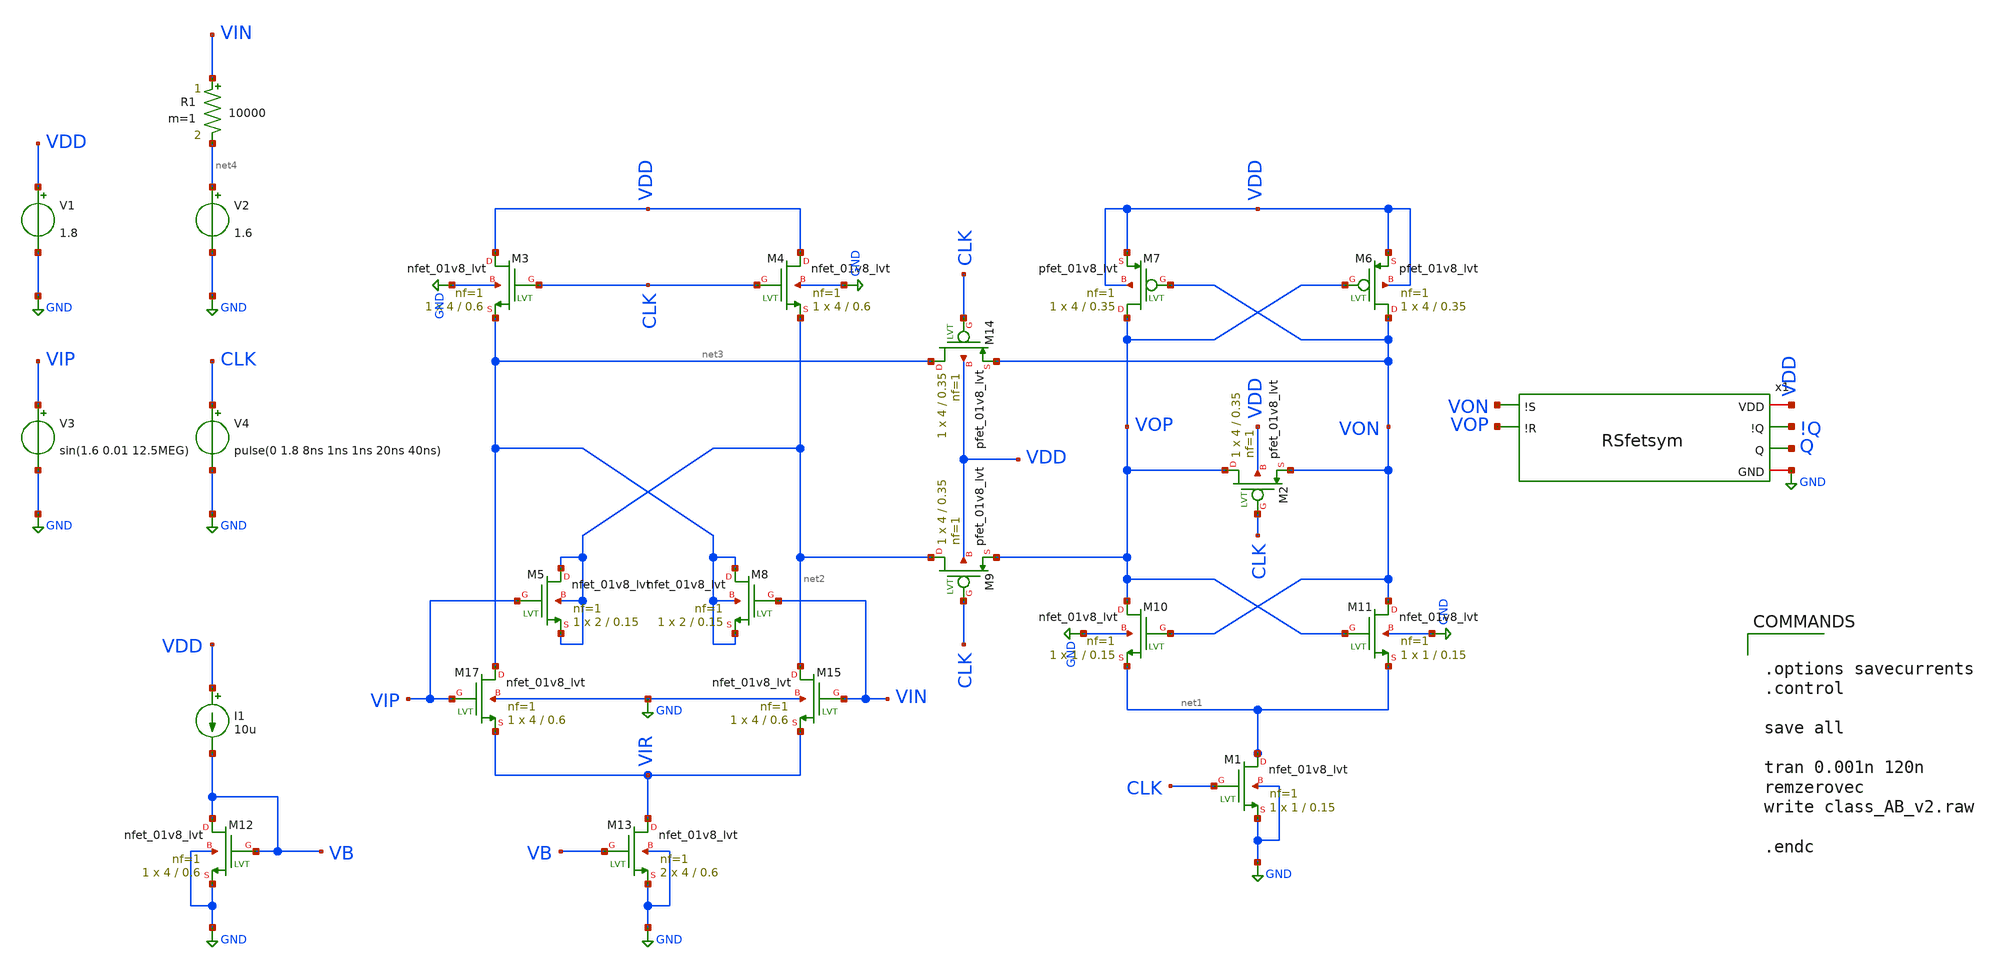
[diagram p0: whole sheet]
** sch_path: testbench/class_AB_v2.sch
.lib $::SKYWATER_MODELS/sky130.lib.spice tt
.include $::SKYWATER_STDCELLS/sky130_fd_sc_hd.spice

**.subckt class_AB_v2
XM17 net3 VIP VIR GND sky130_fd_pr__nfet_01v8_lvt L=0.6 W=4 nf=1 ad='int((nf+1)/2) * W/nf * 0.29' as='int((nf+2)/2) * W/nf * 0.29'
+ pd='2*int((nf+1)/2) * (W/nf + 0.29)' ps='2*int((nf+2)/2) * (W/nf + 0.29)' nrd='0.29 / W' nrs='0.29 / W'
+ sa=0 sb=0 sd=0 mult=1 m=1
XM12 VB VB GND GND sky130_fd_pr__nfet_01v8_lvt L=0.6 W=4 nf=1 ad='int((nf+1)/2) * W/nf * 0.29' as='int((nf+2)/2) * W/nf * 0.29'
+ pd='2*int((nf+1)/2) * (W/nf + 0.29)' ps='2*int((nf+2)/2) * (W/nf + 0.29)' nrd='0.29 / W' nrs='0.29 / W'
+ sa=0 sb=0 sd=0 mult=1 m=1
I1 VDD VB 10u
XM15 net2 VIN VIR GND sky130_fd_pr__nfet_01v8_lvt L=0.6 W=4 nf=1 ad='int((nf+1)/2) * W/nf * 0.29' as='int((nf+2)/2) * W/nf * 0.29'
+ pd='2*int((nf+1)/2) * (W/nf + 0.29)' ps='2*int((nf+2)/2) * (W/nf + 0.29)' nrd='0.29 / W' nrs='0.29 / W'
+ sa=0 sb=0 sd=0 mult=1 m=1
XM13 VIR VB GND GND sky130_fd_pr__nfet_01v8_lvt L=0.6 W=4 nf=1 ad='int((nf+1)/2) * W/nf * 0.29' as='int((nf+2)/2) * W/nf * 0.29'
+ pd='2*int((nf+1)/2) * (W/nf + 0.29)' ps='2*int((nf+2)/2) * (W/nf + 0.29)' nrd='0.29 / W' nrs='0.29 / W'
+ sa=0 sb=0 sd=0 mult=2 m=2
XM6 VON VOP VDD VDD sky130_fd_pr__pfet_01v8_lvt L=0.35 W=4 nf=1 ad='int((nf+1)/2) * W/nf * 0.29' as='int((nf+2)/2) * W/nf * 0.29'
+ pd='2*int((nf+1)/2) * (W/nf + 0.29)' ps='2*int((nf+2)/2) * (W/nf + 0.29)' nrd='0.29 / W' nrs='0.29 / W'
+ sa=0 sb=0 sd=0 mult=1 m=1
XM7 VOP VON VDD VDD sky130_fd_pr__pfet_01v8_lvt L=0.35 W=4 nf=1 ad='int((nf+1)/2) * W/nf * 0.29' as='int((nf+2)/2) * W/nf * 0.29'
+ pd='2*int((nf+1)/2) * (W/nf + 0.29)' ps='2*int((nf+2)/2) * (W/nf + 0.29)' nrd='0.29 / W' nrs='0.29 / W'
+ sa=0 sb=0 sd=0 mult=1 m=1
XM10 VOP VON net1 GND sky130_fd_pr__nfet_01v8_lvt L=0.15 W=1 nf=1 ad='int((nf+1)/2) * W/nf * 0.29' as='int((nf+2)/2) * W/nf * 0.29'
+ pd='2*int((nf+1)/2) * (W/nf + 0.29)' ps='2*int((nf+2)/2) * (W/nf + 0.29)' nrd='0.29 / W' nrs='0.29 / W'
+ sa=0 sb=0 sd=0 mult=1 m=1
XM11 VON VOP net1 GND sky130_fd_pr__nfet_01v8_lvt L=0.15 W=1 nf=1 ad='int((nf+1)/2) * W/nf * 0.29' as='int((nf+2)/2) * W/nf * 0.29'
+ pd='2*int((nf+1)/2) * (W/nf + 0.29)' ps='2*int((nf+2)/2) * (W/nf + 0.29)' nrd='0.29 / W' nrs='0.29 / W'
+ sa=0 sb=0 sd=0 mult=1 m=1
XM1 net1 CLK GND GND sky130_fd_pr__nfet_01v8_lvt L=0.15 W=1 nf=1 ad='int((nf+1)/2) * W/nf * 0.29' as='int((nf+2)/2) * W/nf * 0.29'
+ pd='2*int((nf+1)/2) * (W/nf + 0.29)' ps='2*int((nf+2)/2) * (W/nf + 0.29)' nrd='0.29 / W' nrs='0.29 / W'
+ sa=0 sb=0 sd=0 mult=1 m=1
XM2 VOP CLK VON VDD sky130_fd_pr__pfet_01v8_lvt L=0.35 W=4 nf=1 ad='int((nf+1)/2) * W/nf * 0.29' as='int((nf+2)/2) * W/nf * 0.29'
+ pd='2*int((nf+1)/2) * (W/nf + 0.29)' ps='2*int((nf+2)/2) * (W/nf + 0.29)' nrd='0.29 / W' nrs='0.29 / W'
+ sa=0 sb=0 sd=0 mult=1 m=1
V1 VDD GND 1.8
V3 VIP GND sin(1.6 0.01 12.5MEG)
V2 net4 GND 1.6
V4 CLK GND pulse(0 1.8 8ns 1ns 1ns 20ns 40ns)
R1 VIN net4 10000 m=1
XM5 net2 VIP net2 net2 sky130_fd_pr__nfet_01v8_lvt L=0.15 W=2 nf=1 ad='int((nf+1)/2) * W/nf * 0.29' as='int((nf+2)/2) * W/nf * 0.29'
+ pd='2*int((nf+1)/2) * (W/nf + 0.29)' ps='2*int((nf+2)/2) * (W/nf + 0.29)' nrd='0.29 / W' nrs='0.29 / W'
+ sa=0 sb=0 sd=0 mult=1 m=1
XM8 net3 VIN net3 net3 sky130_fd_pr__nfet_01v8_lvt L=0.15 W=2 nf=1 ad='int((nf+1)/2) * W/nf * 0.29' as='int((nf+2)/2) * W/nf * 0.29'
+ pd='2*int((nf+1)/2) * (W/nf + 0.29)' ps='2*int((nf+2)/2) * (W/nf + 0.29)' nrd='0.29 / W' nrs='0.29 / W'
+ sa=0 sb=0 sd=0 mult=1 m=1
XM9 net2 CLK VOP VDD sky130_fd_pr__pfet_01v8_lvt L=0.35 W=4 nf=1 ad='int((nf+1)/2) * W/nf * 0.29' as='int((nf+2)/2) * W/nf * 0.29'
+ pd='2*int((nf+1)/2) * (W/nf + 0.29)' ps='2*int((nf+2)/2) * (W/nf + 0.29)' nrd='0.29 / W' nrs='0.29 / W'
+ sa=0 sb=0 sd=0 mult=1 m=1
XM14 net3 CLK VON VDD sky130_fd_pr__pfet_01v8_lvt L=0.35 W=4 nf=1 ad='int((nf+1)/2) * W/nf * 0.29' as='int((nf+2)/2) * W/nf * 0.29'
+ pd='2*int((nf+1)/2) * (W/nf + 0.29)' ps='2*int((nf+2)/2) * (W/nf + 0.29)' nrd='0.29 / W' nrs='0.29 / W'
+ sa=0 sb=0 sd=0 mult=1 m=1
XM3 VDD CLK net3 GND sky130_fd_pr__nfet_01v8_lvt L=0.6 W=4 nf=1 ad='int((nf+1)/2) * W/nf * 0.29' as='int((nf+2)/2) * W/nf * 0.29'
+ pd='2*int((nf+1)/2) * (W/nf + 0.29)' ps='2*int((nf+2)/2) * (W/nf + 0.29)' nrd='0.29 / W' nrs='0.29 / W'
+ sa=0 sb=0 sd=0 mult=1 m=1
XM4 VDD CLK net2 GND sky130_fd_pr__nfet_01v8_lvt L=0.6 W=4 nf=1 ad='int((nf+1)/2) * W/nf * 0.29' as='int((nf+2)/2) * W/nf * 0.29'
+ pd='2*int((nf+1)/2) * (W/nf + 0.29)' ps='2*int((nf+2)/2) * (W/nf + 0.29)' nrd='0.29 / W' nrs='0.29 / W'
+ sa=0 sb=0 sd=0 mult=1 m=1
x1 VDD VON VOP !Q Q GND RSfetsym
**** begin user architecture code


.options savecurrents
.control

save all

tran 0.001n 120n
remzerovec
write class_AB_v2.raw

.endc


**** end user architecture code
**.ends
.GLOBAL GND
.end
